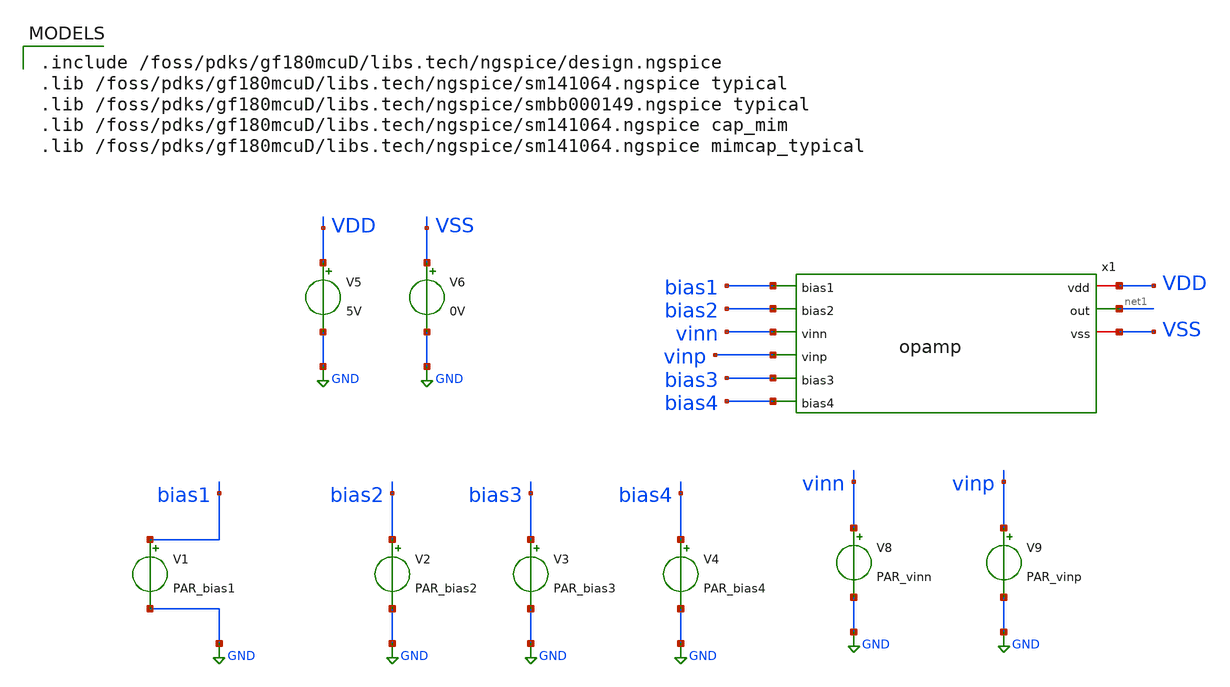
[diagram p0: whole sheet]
** sch_path: activities/opamp2AKAM/simulations_testbench/simulations_testbench/testBenchOpamp.sch
**.subckt testBenchOpamp
V1 bias1 GND PAR_bias1
V2 bias2 GND PAR_bias2
V3 bias3 GND PAR_bias3
V4 bias4 GND PAR_bias4
V5 VDD GND 5V
V6 VSS GND 0V
V8 vinn GND PAR_vinn
V9 vinp GND PAR_vinp
x1 VDD bias1 bias2 vinn net1 vinp bias3 bias4 VSS opamp
**** begin user architecture code

.include /foss/pdks/gf180mcuD/libs.tech/ngspice/design.ngspice
.lib /foss/pdks/gf180mcuD/libs.tech/ngspice/sm141064.ngspice typical
.lib /foss/pdks/gf180mcuD/libs.tech/ngspice/smbb000149.ngspice typical
.lib /foss/pdks/gf180mcuD/libs.tech/ngspice/sm141064.ngspice cap_mim
.lib /foss/pdks/gf180mcuD/libs.tech/ngspice/sm141064.ngspice mimcap_typical


** PARAMETERS
.PARAM PAR_bias1=3.425
.PARAM PAR_bias2=3.425
.PARAM PAR_bias3=3.425
.PARAM PAR_bias4=3.425
.PARAM PAR_vinn=2.5
.PARAM PAR_vinp=2.5

.control
  * clear the results file and write a header row
  echo "# bias1 bias2 bias3 bias4 gain" >
+ /foss/designs/sscs-2026-zotnetic/activities/opamp2AKAM/simulations_testbench/simulation_results/sweep_results.txt

  * ---- OUTER LOOP: try many bias combinations ----
  * nominal point is 3.425 / 2.428 / 1.909 / 1.209.
  * (the +0.001 on each limit dodges float-rounding overshoot)
  let b1 = 3.0
  while b1 <= 3.801
    let b2 = 2.2
    while b2 <= 2.601
      let b3 = 1.7
      while b3 <= 2.101
        let b4 = 1.0
        while b4 <= 1.401

          * set the four bias knobs for this combination
          alter V1 = b1
          alter V2 = b2
          alter V3 = b3
          alter V4 = b4

          * ---- INNER LOOP: sweep the input to measure gain ----
          dc V9 0 5 0.001

          * read the slope: input where output passes 1.5 V and 3.5 V
          meas dc vlo when v(net1)=1.5 cross=1
          meas dc vhi when v(net1)=3.5 cross=1
          let gain = 2.0/abs(vhi-vlo)

          * write one row of the table
          echo "$&b1 $&b2 $&b3 $&b4 $&gain" >>
+ /foss/designs/sscs-2026-zotnetic/activities/opamp2AKAM/simulations_testbench/simulation_results/sweep_results.txt

          let b4 = b4 + 0.2
        end
        let b3 = b3 + 0.2
      end
      let b2 = b2 + 0.2
    end
    let b1 = b1 + 0.2
  end

  echo "DONE - results in sweep_results.txt"
.endc

**** end user architecture code
**.ends
.GLOBAL GND
.end
